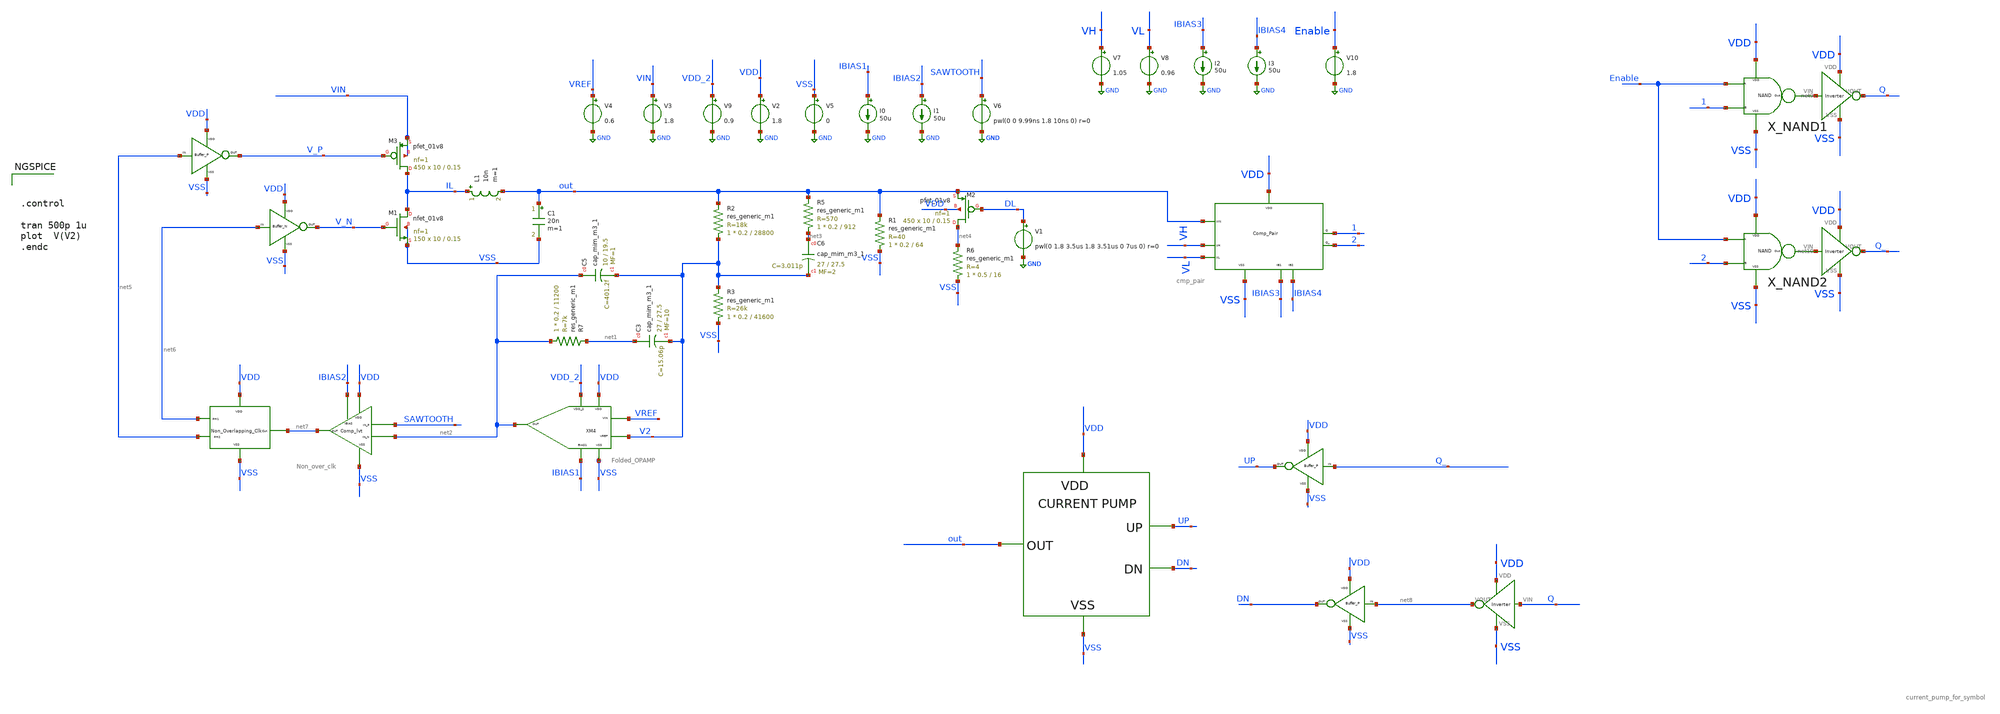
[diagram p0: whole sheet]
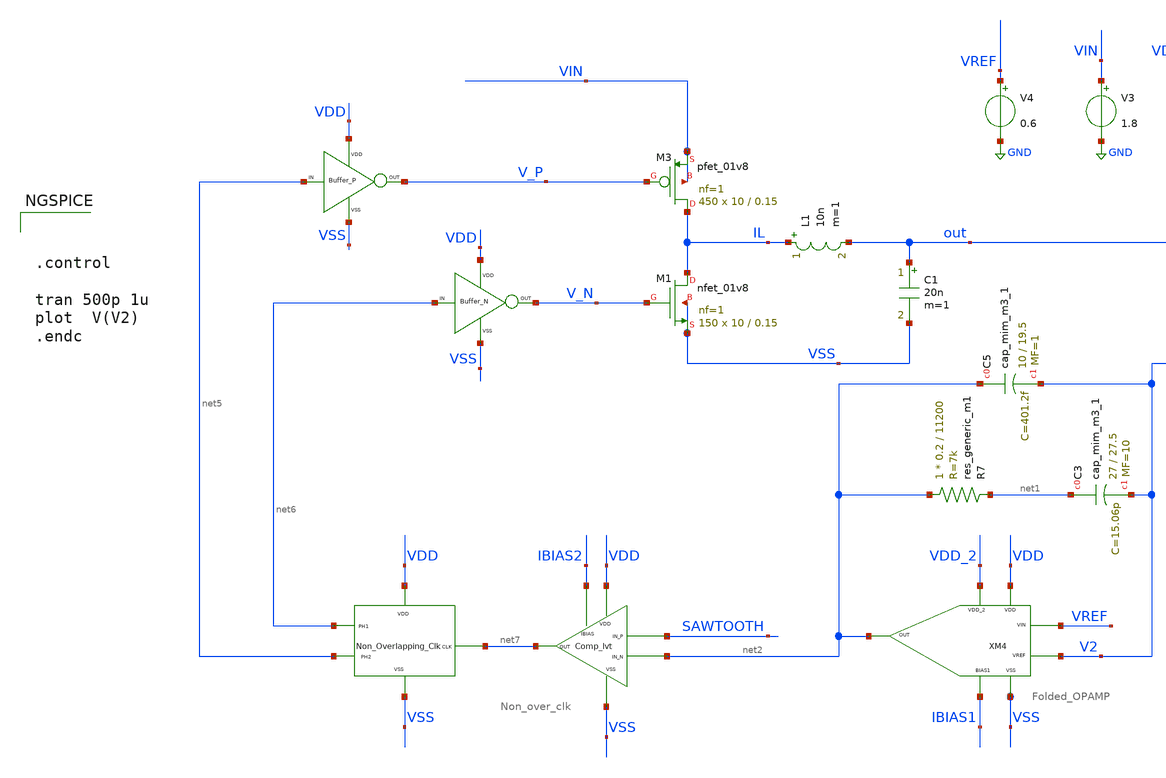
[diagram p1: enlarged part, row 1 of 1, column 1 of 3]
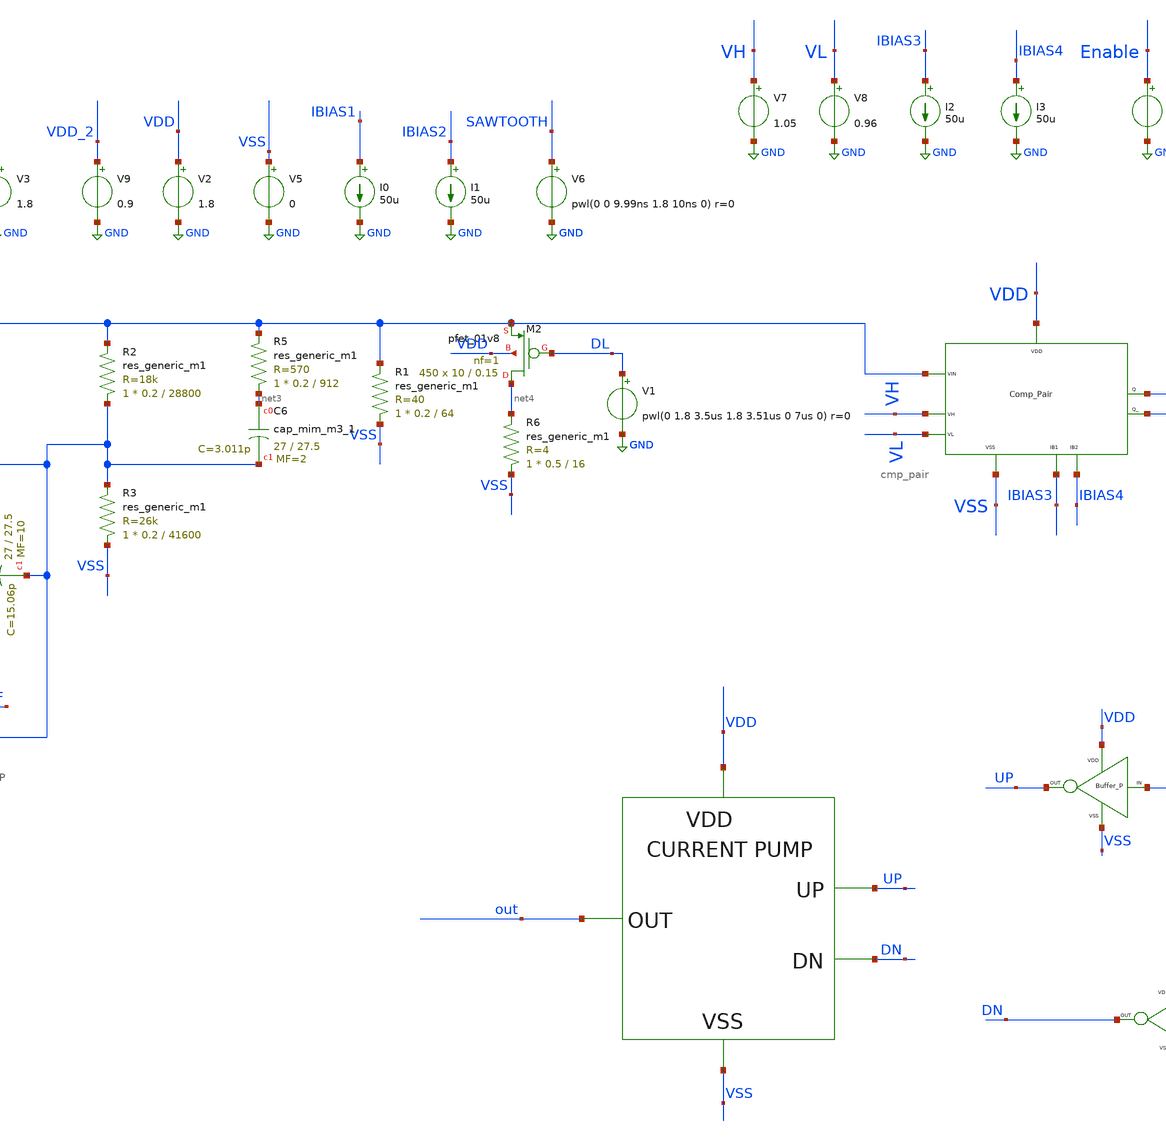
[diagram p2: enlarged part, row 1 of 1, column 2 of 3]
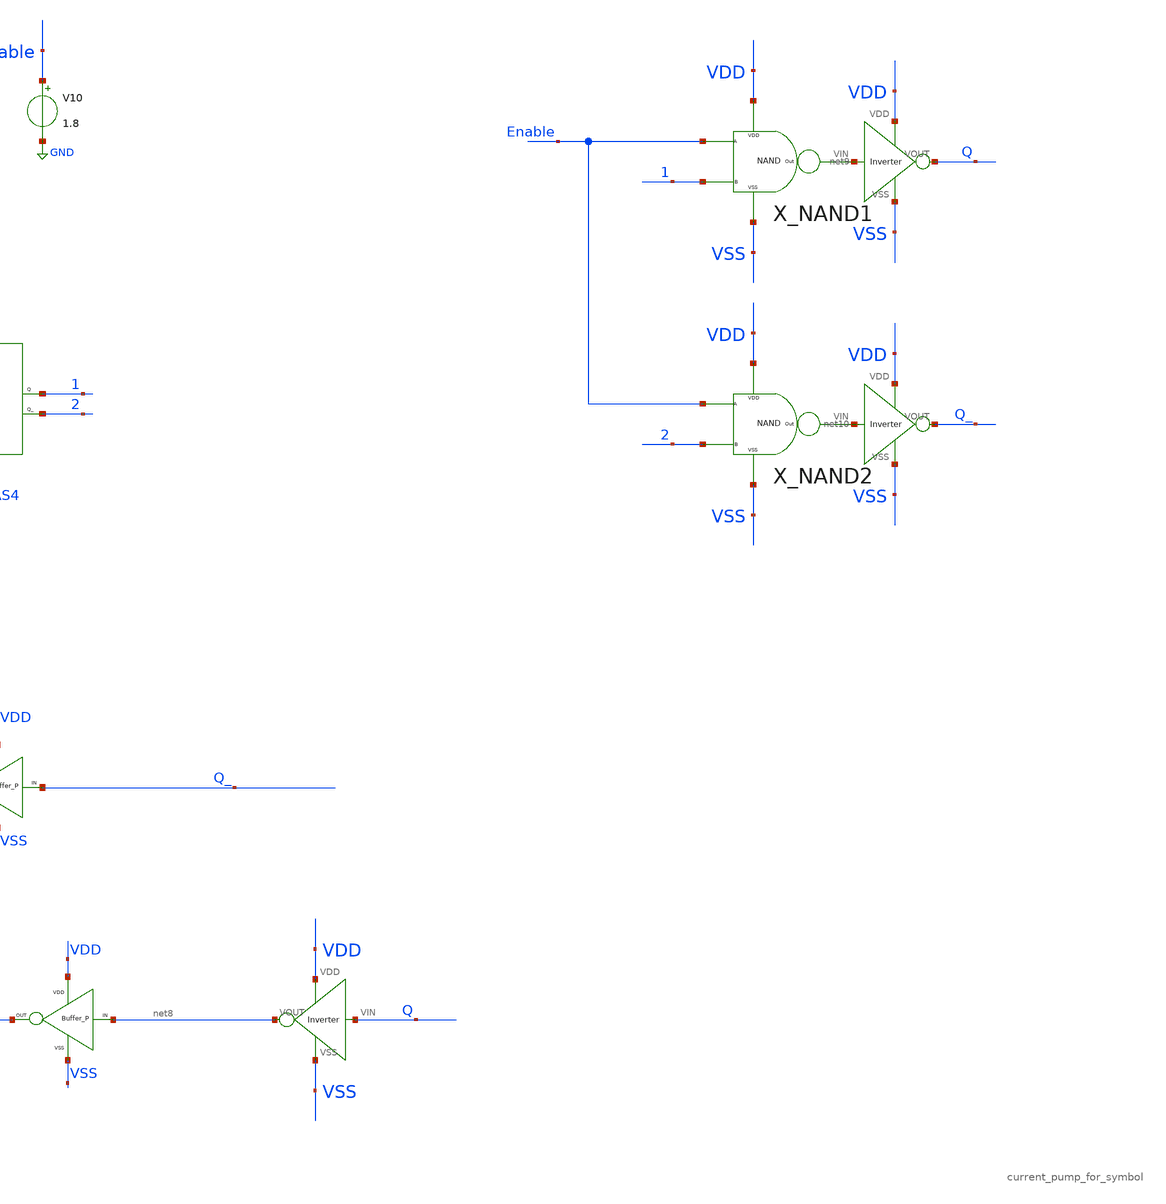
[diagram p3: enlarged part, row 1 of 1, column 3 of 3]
** sch_path: xschem/DC_DC_Converter_xschem/OTHERS/DC_DC_Converter_4/Folded_OPAMP/rough.sch
**.subckt rough
XM3 IL V_P VIN VIN sky130_fd_pr__pfet_01v8 L=0.15 W=10 nf=1 ad='int((nf+1)/2) * W/nf * 0.29' as='int((nf+2)/2) * W/nf * 0.29'
+ pd='2*int((nf+1)/2) * (W/nf + 0.29)' ps='2*int((nf+2)/2) * (W/nf + 0.29)' nrd='0.29 / W' nrs='0.29 / W'
+ sa=0 sb=0 sd=0 mult=450 m=450
L1 IL out 10n m=1
C1 out VSS 20n m=1
V3 VIN GND 1.8
I0 IBIAS1 GND 50u
V9 VDD_2 GND 0.9
V2 VDD GND 1.8
V5 VSS GND 0
V4 VREF GND 0.6
I1 IBIAS2 GND 50u
V6 SAWTOOTH GND pwl(0 0 9.99ns 1.8 10ns 0) r=0
XM1 IL V_N VSS VSS sky130_fd_pr__nfet_01v8 L=0.15 W=10 nf=1 ad='int((nf+1)/2) * W/nf * 0.29' as='int((nf+2)/2) * W/nf * 0.29'
+ pd='2*int((nf+1)/2) * (W/nf + 0.29)' ps='2*int((nf+2)/2) * (W/nf + 0.29)' nrd='0.29 / W' nrs='0.29 / W'
+ sa=0 sb=0 sd=0 mult=150 m=150
XM2 net4 DL out VDD sky130_fd_pr__pfet_01v8 L=0.15 W=10 nf=1 ad='int((nf+1)/2) * W/nf * 0.29' as='int((nf+2)/2) * W/nf * 0.29'
+ pd='2*int((nf+1)/2) * (W/nf + 0.29)' ps='2*int((nf+2)/2) * (W/nf + 0.29)' nrd='0.29 / W' nrs='0.29 / W'
+ sa=0 sb=0 sd=0 mult=450 m=450
V1 DL GND pwl(0 1.8 3.5us 1.8 3.51us 0 7us 0) r=0
X1 net5 V_P VDD VSS BUFFER_P
X2 net6 V_N VDD VSS BUFFER_N
XM3 net7 VDD VSS net6 net5 Non_over_clk
XM4 VDD VSS VDD_2 IBIAS1 net2 VREF V2 Folded_OPAMP
XM2 IBIAS2 VDD SAWTOOTH net2 VSS net7 Comp_lvt
V7 VH GND 1.05
V8 VL GND 0.96
I2 IBIAS3 GND 50u
I3 IBIAS4 GND 50u
XM1 VDD VSS out VH VL IBIAS3 IBIAS4 1 2 cmp_pair
X5 net8 DN VDD VSS BUFFER_P
X6 Q_ UP VDD VSS BUFFER_P
X7 UP out VDD VSS DN current_pump_for_symbol
X_NAND1 VDD VSS Enable 1 net9 NAND
X_NAND2 VDD VSS Enable 2 net10 NAND
X9 VSS VDD net9 Q Inverter
X10 VSS VDD net10 Q_ Inverter
XC5 net2 V2 sky130_fd_pr__cap_mim_m3_1 W=10 L=19.5 MF=1 m=1
XC3 net1 V2 sky130_fd_pr__cap_mim_m3_1 W=27 L=27.5 MF=10 m=10
R7 net2 net1 sky130_fd_pr__res_generic_m1 W=0.2 L=11200 m=1
R6 VSS net4 sky130_fd_pr__res_generic_m1 W=0.5 L=16 m=1
R1 VSS out sky130_fd_pr__res_generic_m1 W=0.2 L=64 m=1
R5 net3 out sky130_fd_pr__res_generic_m1 W=0.2 L=912 m=1
R2 V2 out sky130_fd_pr__res_generic_m1 W=0.2 L=28800 m=1
R3 VSS V2 sky130_fd_pr__res_generic_m1 W=0.2 L=41600 m=1
V10 Enable GND 1.8
XC6 net3 V2 sky130_fd_pr__cap_mim_m3_1 W=27 L=27.5 MF=2 m=2
X3 VSS VDD Q net8 Inverter
**** begin user architecture code

** opencircuitdesign pdks install
.lib $::SKYWATER_MODELS/sky130.lib.spice tt





.control

tran 500p 1u
plot  V(V2)
.endc


**** end user architecture code
**.ends
.GLOBAL GND
.end
